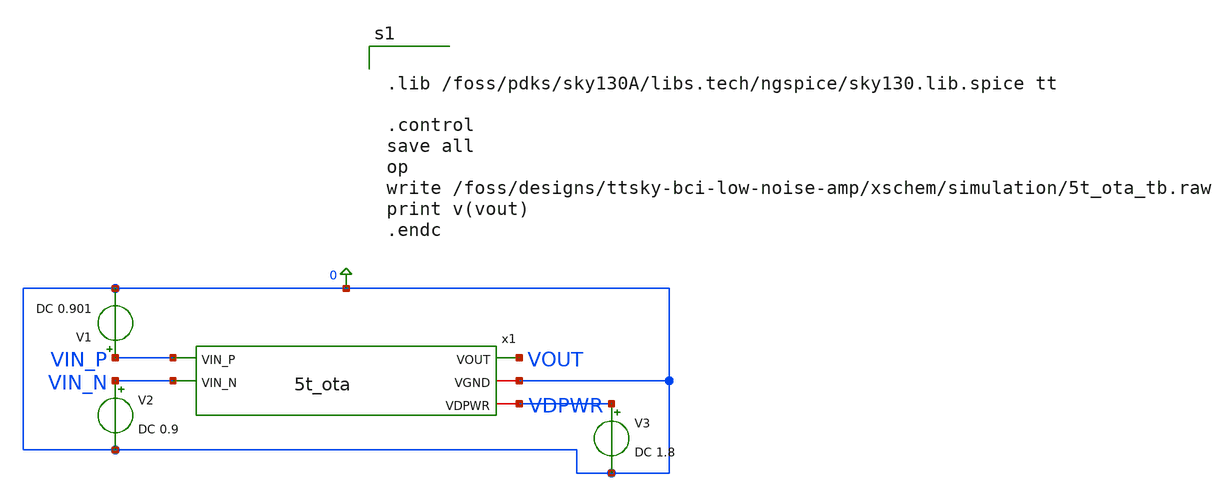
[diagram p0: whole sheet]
** sch_path: xschem/5t_ota_tb.sch
**.subckt 5t_ota_tb
V1 VIN_P 0 DC 0.901
V2 VIN_N 0 DC 0.9
V3 VDPWR 0 DC 1.8
x1 VOUT 0 VIN_P VIN_N VDPWR 5t_ota
**** begin user architecture code


.lib /foss/pdks/sky130A/libs.tech/ngspice/sky130.lib.spice tt

.control
save all
op
write /foss/designs/ttsky-bci-low-noise-amp/xschem/simulation/5t_ota_tb.raw
print v(vout)
.endc


**** end user architecture code
**.ends

* expanding   symbol:  /foss/designs/ttsky-bci-low-noise-amp/xschem/5t_ota.sym # of pins=5
** sym_path: xschem/5t_ota.sym
** sch_path: xschem/5t_ota.sch
.subckt 5t_ota VOUT VGND VIN_P VIN_N VDPWR
*.iopin VGND
*.ipin VIN_N
*.ipin VIN_P
*.iopin VDPWR
*.opin VOUT
MM1 net1 net1 VGND VGND sky130_fd_pr__nfet_01v8 L=0.15 W=1 nf=1 ad='int((1 + 1)/2) * 1 / 1 * 0.29' as='int((1 + 2)/2) * 1 / 1 * 0.29'
+ pd='2*int((1 + 1)/2) * (1 / 1 + 0.29)' ps='2*int((1 + 2)/2) * (1 / 1 + 0.29)' nrd='0.29 / 1 ' nrs='0.29 / 1 '
+ sa=0 sb=0 sd=0 mult=1 m=1
MM2 VOUT net1 VGND VGND sky130_fd_pr__nfet_01v8 L=0.15 W=1 nf=1 ad='int((1 + 1)/2) * 1 / 1 * 0.29' as='int((1 + 2)/2) * 1 / 1 * 0.29'
+ pd='2*int((1 + 1)/2) * (1 / 1 + 0.29)' ps='2*int((1 + 2)/2) * (1 / 1 + 0.29)' nrd='0.29 / 1 ' nrs='0.29 / 1 '
+ sa=0 sb=0 sd=0 mult=1 m=1
MM3 net1 VIN_P net2 VDPWR sky130_fd_pr__pfet_01v8 L=0.15 W=1 nf=1 ad='int((1 + 1)/2) * 1 / 1 * 0.29'
+ as='int((1 + 2)/2) * 1 / 1 * 0.29' pd='2*int((1 + 1)/2) * (1 / 1 + 0.29)' ps='2*int((1 + 2)/2) * (1 / 1 + 0.29)'
+ nrd='0.29 / 1 ' nrs='0.29 / 1 ' sa=0 sb=0 sd=0 mult=1 m=1
MM4 VOUT VIN_N net2 VDPWR sky130_fd_pr__pfet_01v8 L=0.15 W=1 nf=1 ad='int((1 + 1)/2) * 1 / 1 * 0.29'
+ as='int((1 + 2)/2) * 1 / 1 * 0.29' pd='2*int((1 + 1)/2) * (1 / 1 + 0.29)' ps='2*int((1 + 2)/2) * (1 / 1 + 0.29)'
+ nrd='0.29 / 1 ' nrs='0.29 / 1 ' sa=0 sb=0 sd=0 mult=1 m=1
MM5 net2 net3 VDPWR VDPWR sky130_fd_pr__pfet_01v8 L=0.15 W=1 nf=1 ad='int((1 + 1)/2) * 1 / 1 * 0.29'
+ as='int((1 + 2)/2) * 1 / 1 * 0.29' pd='2*int((1 + 1)/2) * (1 / 1 + 0.29)' ps='2*int((1 + 2)/2) * (1 / 1 + 0.29)'
+ nrd='0.29 / 1 ' nrs='0.29 / 1 ' sa=0 sb=0 sd=0 mult=1 m=1
MM6 net3 net3 VDPWR VDPWR sky130_fd_pr__pfet_01v8 L=0.15 W=1 nf=1 ad='int((1 + 1)/2) * 1 / 1 * 0.29'
+ as='int((1 + 2)/2) * 1 / 1 * 0.29' pd='2*int((1 + 1)/2) * (1 / 1 + 0.29)' ps='2*int((1 + 2)/2) * (1 / 1 + 0.29)'
+ nrd='0.29 / 1 ' nrs='0.29 / 1 ' sa=0 sb=0 sd=0 mult=1 m=1
MM7 net3 net3 VGND VGND sky130_fd_pr__nfet_01v8 L=0.15 W=1 nf=1 ad='int((1 + 1)/2) * 1 / 1 * 0.29' as='int((1 + 2)/2) * 1 / 1 * 0.29'
+ pd='2*int((1 + 1)/2) * (1 / 1 + 0.29)' ps='2*int((1 + 2)/2) * (1 / 1 + 0.29)' nrd='0.29 / 1 ' nrs='0.29 / 1 '
+ sa=0 sb=0 sd=0 mult=1 m=1
.ends

.end
